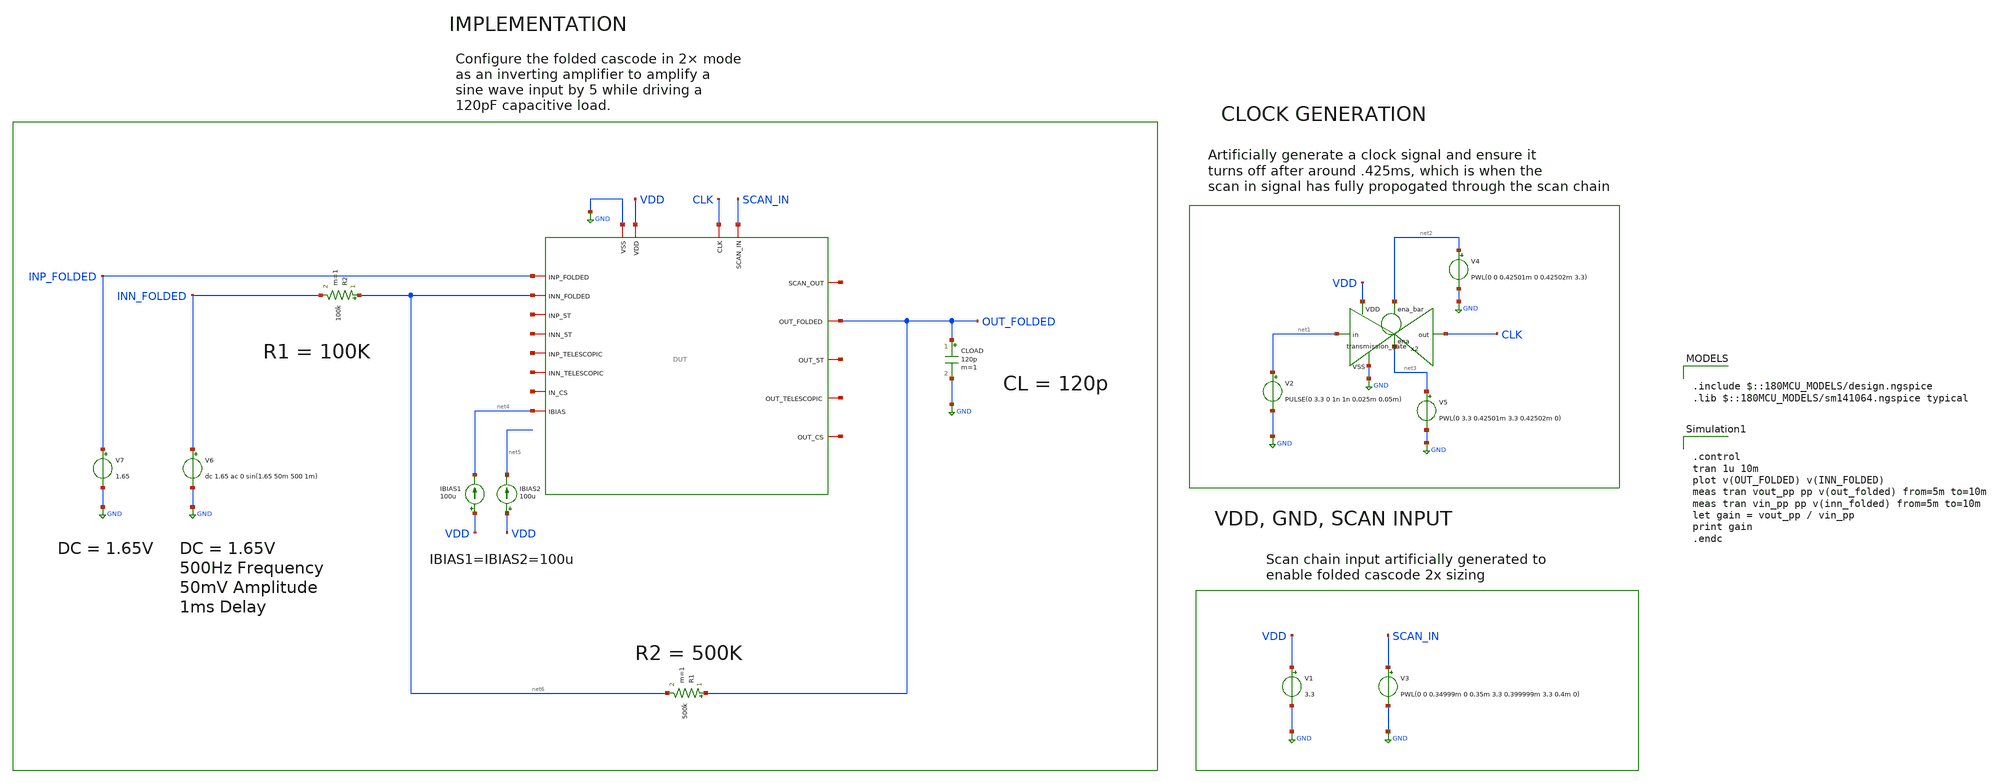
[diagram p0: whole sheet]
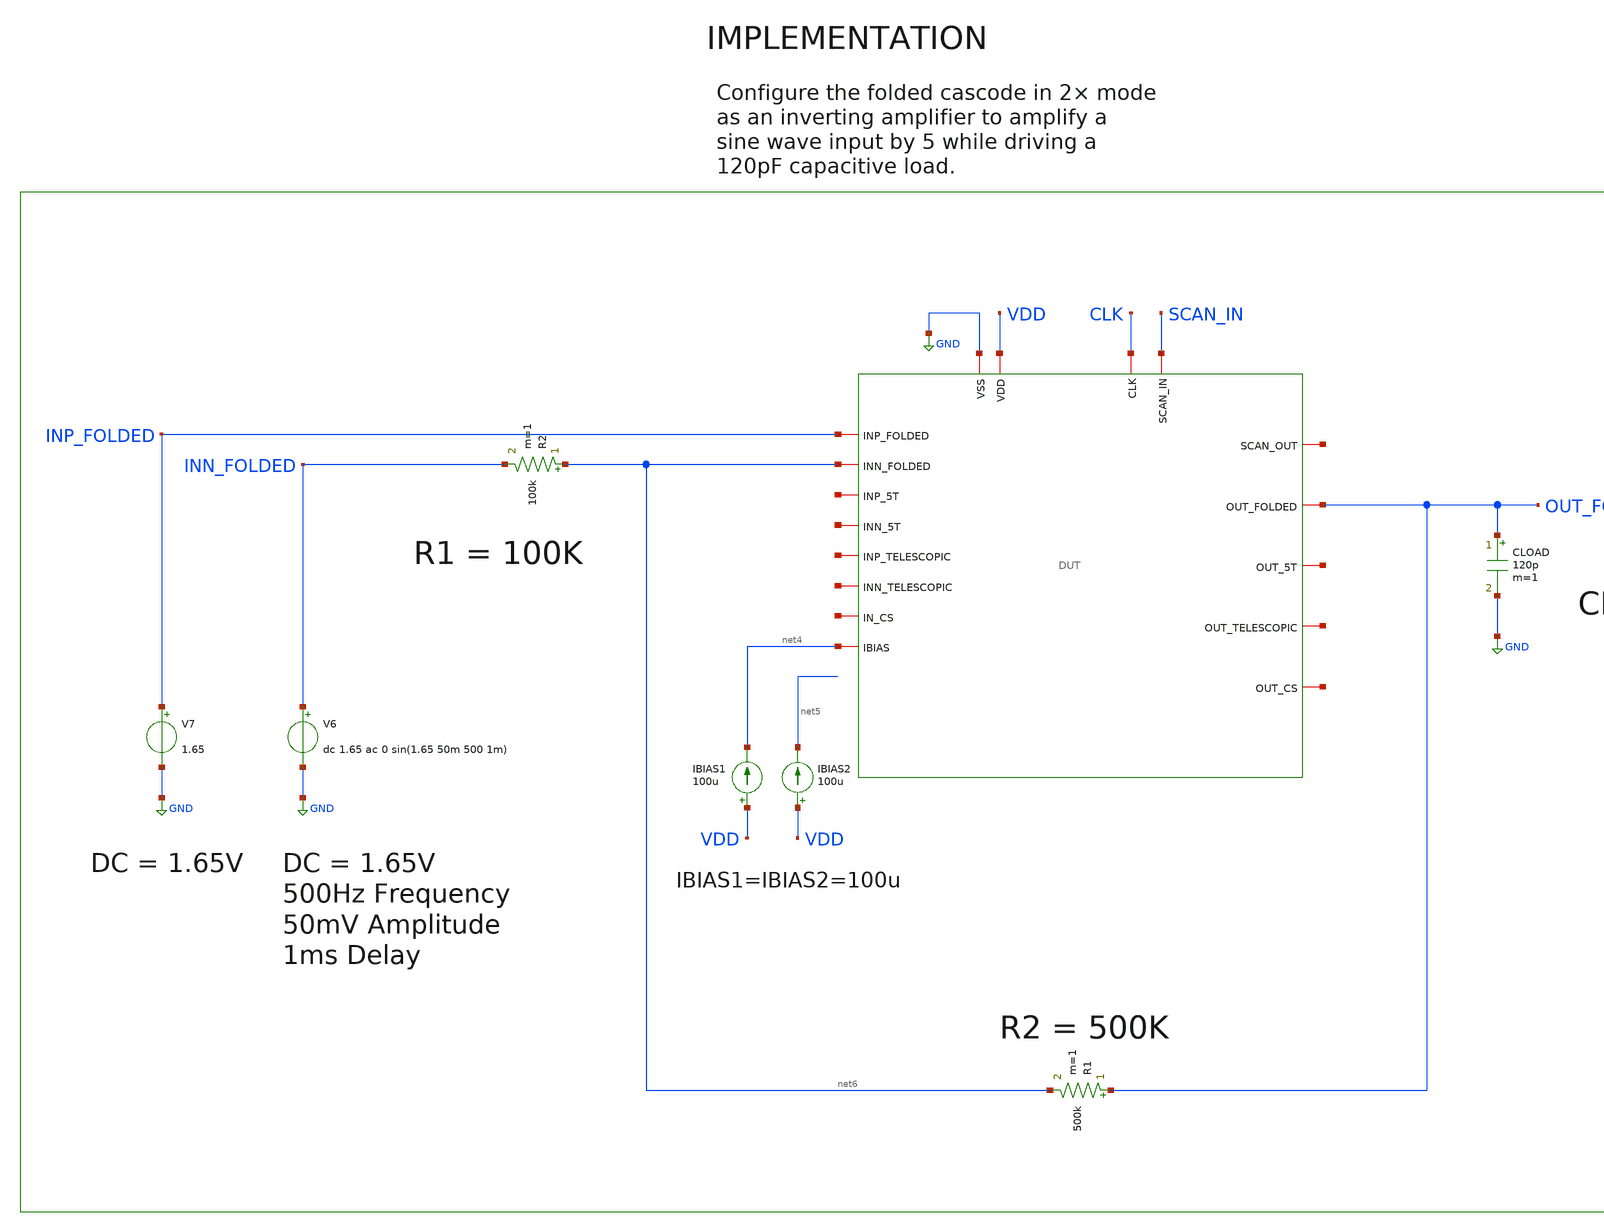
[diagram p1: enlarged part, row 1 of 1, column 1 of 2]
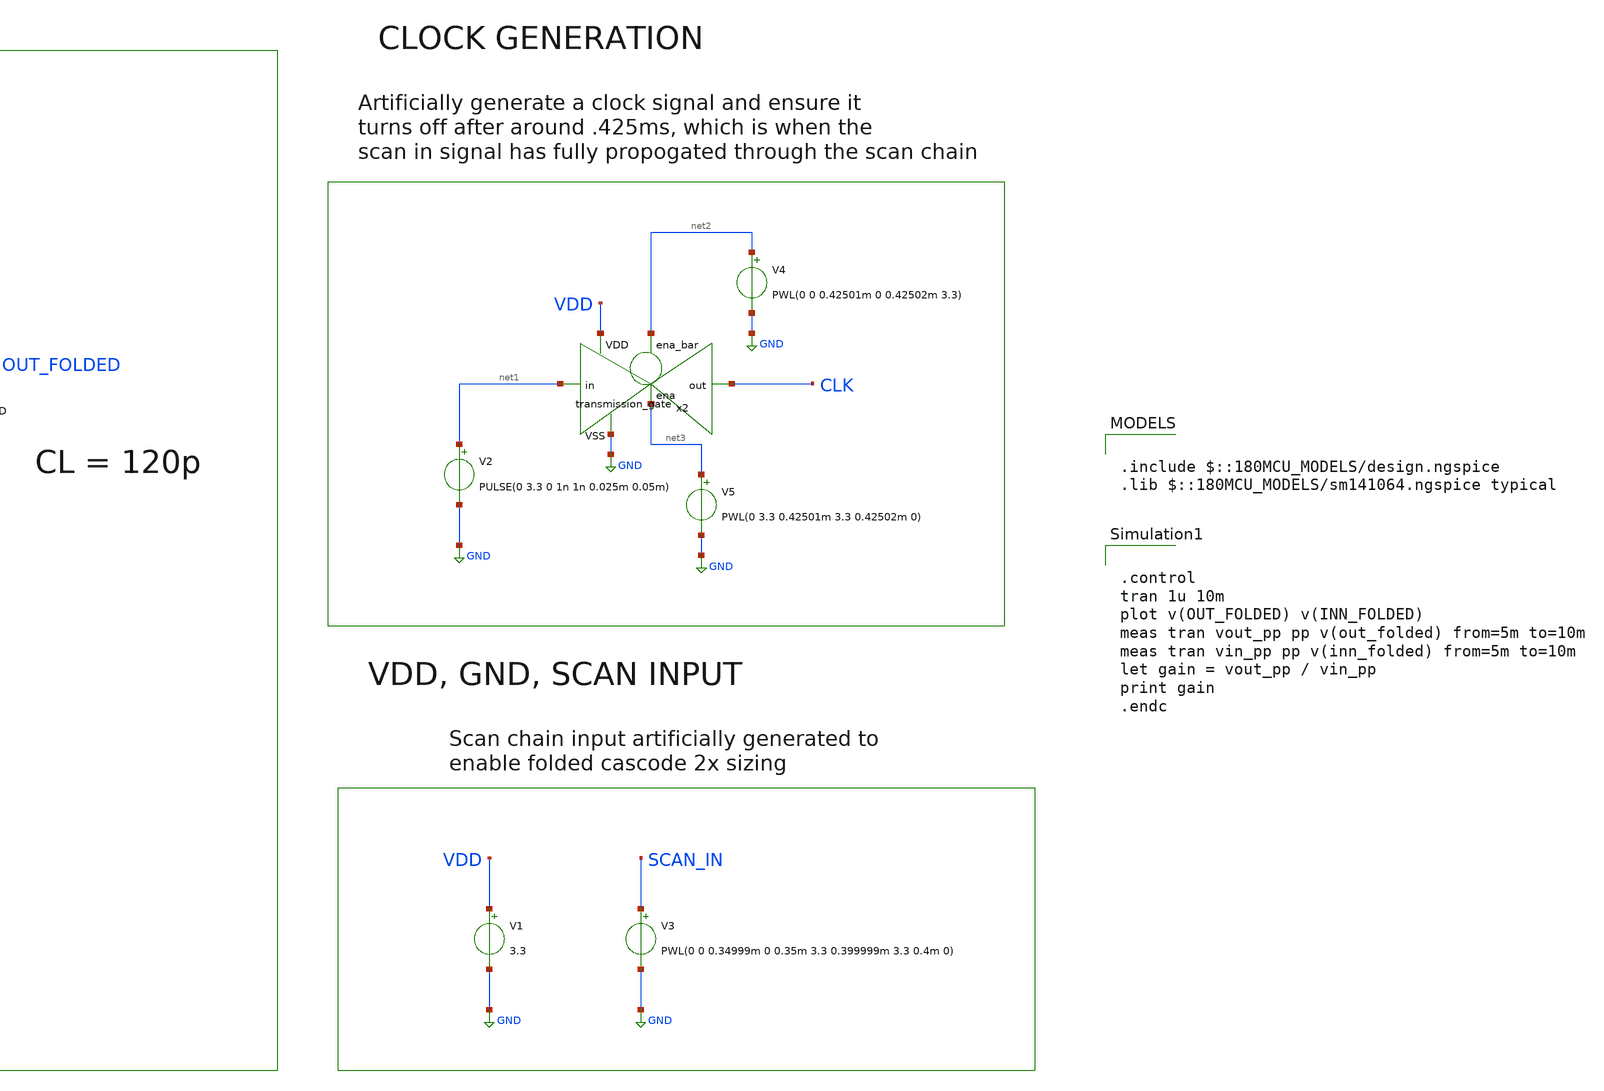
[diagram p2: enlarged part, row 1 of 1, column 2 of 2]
** sch_path: designs/libs/core_tb/etj/ota_folded/inverting_amp/input_sine_2x.sch
**.subckt input_sine_2x
V3 SCAN_IN GND PWL(0 0 0.34999m 0 0.35m 3.3 0.399999m 3.3 0.4m 0)
V1 VDD GND 3.3
V2 net1 GND PULSE(0 3.3 0 1n 1n 0.025m 0.05m)
x2 net2 VDD CLK net1 GND net3 transmission_gate
V4 net2 GND PWL(0 0 0.42501m 0 0.42502m 3.3)
V5 net3 GND PWL(0 3.3 0.42501m 3.3 0.42502m 0)
IBIAS1 VDD net4 100u
IBIAS2 VDD net5 100u
V7 INP_FOLDED GND 1.65
CLOAD OUT_FOLDED GND 120p m=1
R2 net6 INN_FOLDED 100k m=1
V6 INN_FOLDED GND dc 1.65 ac 0 sin(1.65 50m 500 1m)
R1 OUT_FOLDED net6 500k m=1
x1 CLK net7 SCAN_IN GND VDD OUT_FOLDED INP_FOLDED net8 net4 net6 net9 net10 net11 net12 net13 net14
+ net15 DUT
**** begin user architecture code

.include $::180MCU_MODELS/design.ngspice
.lib $::180MCU_MODELS/sm141064.ngspice typical



.control
tran 1u 10m
plot v(OUT_FOLDED) v(INN_FOLDED)
meas tran vout_pp pp v(out_folded) from=5m to=10m
meas tran vin_pp pp v(inn_folded) from=5m to=10m
let gain = vout_pp / vin_pp
print gain
.endc


**** end user architecture code
**.ends
.GLOBAL GND
.end
